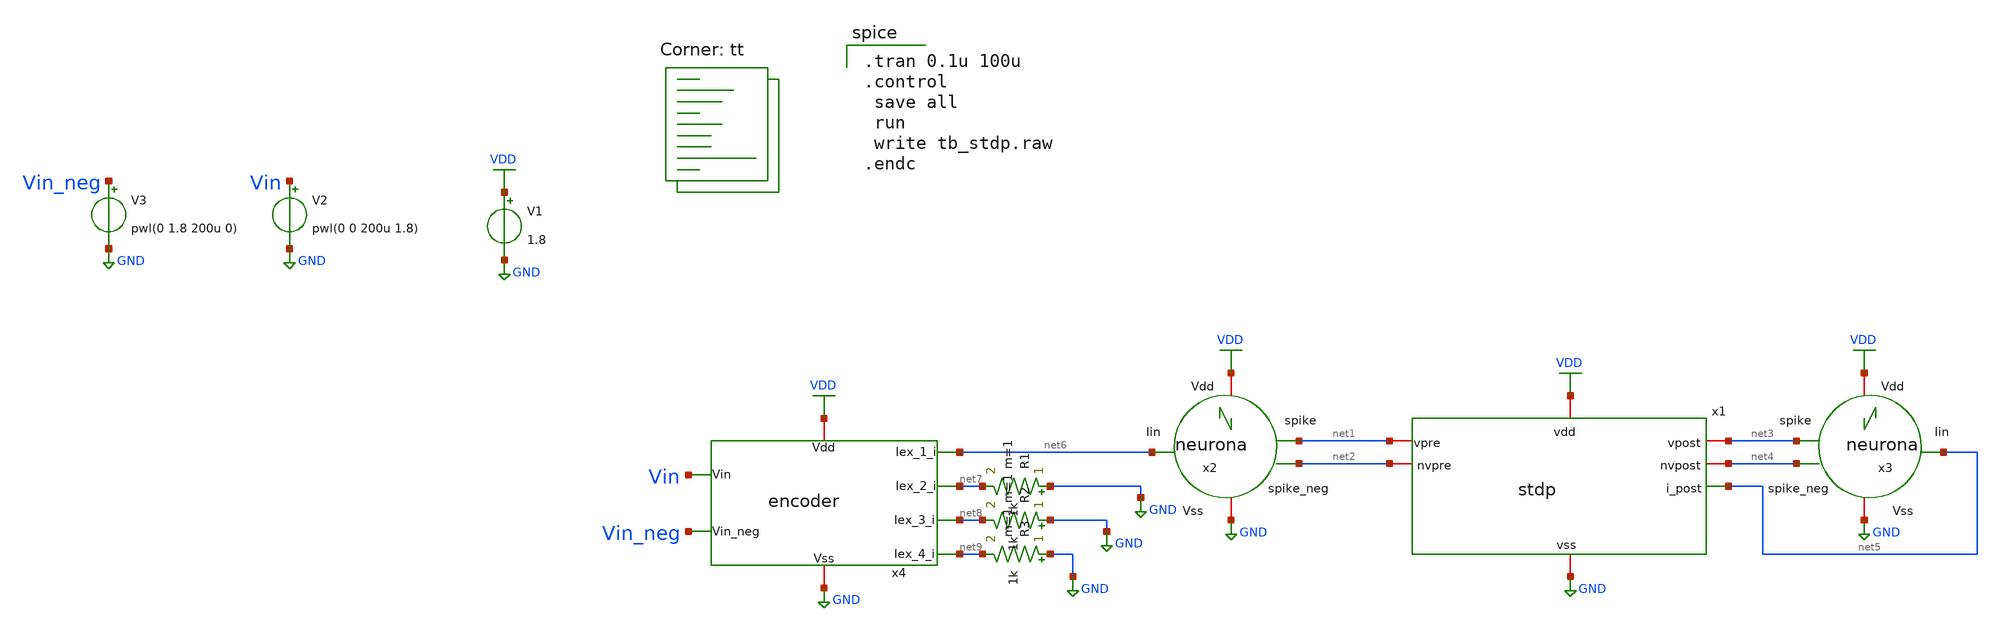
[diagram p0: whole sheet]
** sch_path: designs/libs/snn_analog/stdp/sch/tb_stdp.sch
**.subckt tb_stdp
x1 VDD GND net5 net1 net2 net4 net3 stdp
x2 net6 VDD GND net1 net2 neurona
x3 net5 VDD GND net3 net4 neurona
x4 VDD GND Vin Vin_neg net6 net7 net8 net9 encoder
V1 VDD GND 1.8
V2 Vin GND pwl(0 0 200u 1.8)
V3 Vin_neg GND pwl(0 1.8 200u 0)
R2 GND net8 1k m=1
R3 GND net9 1k m=1
R1 GND net7 1k m=1
**** begin user architecture code
.lib $::SKYWATER_MODELS/sky130.lib.spice tt

.tran 0.1u 100u
.control
 save all
 run
 write tb_stdp.raw
.endc

**** end user architecture code
**.ends
.GLOBAL GND
.GLOBAL VDD
.end
